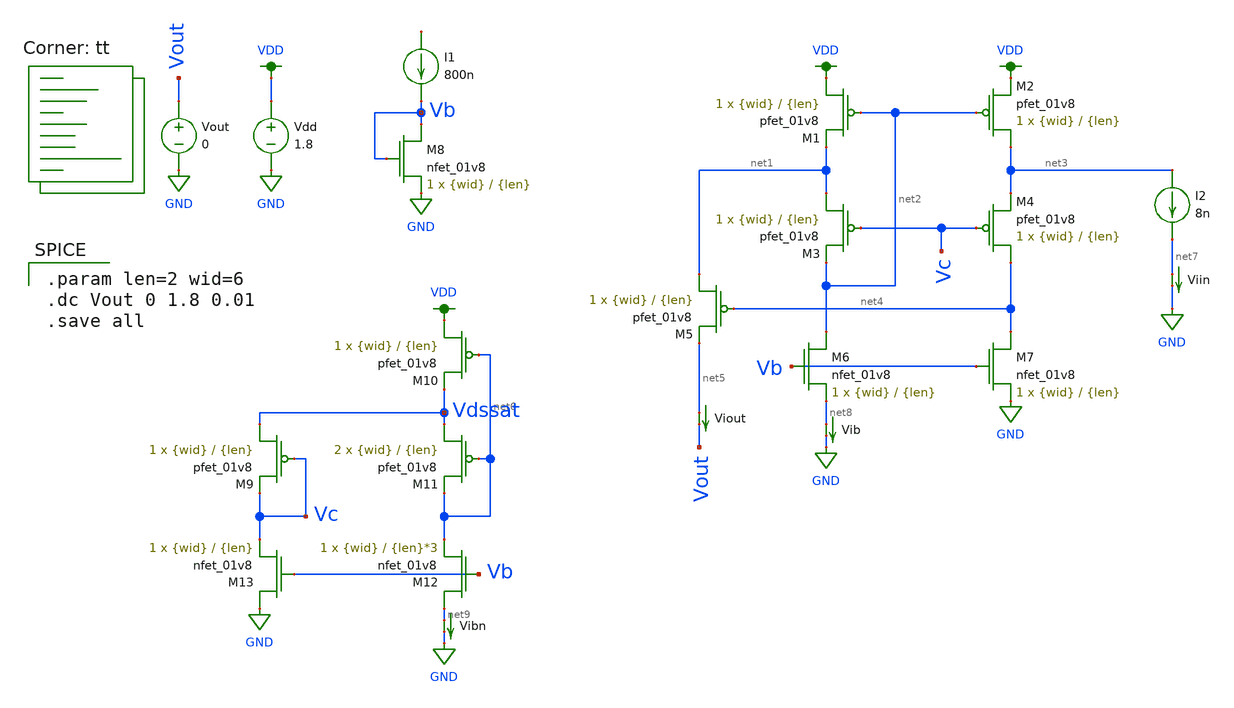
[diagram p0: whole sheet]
** sch_path: mp3/mirror_tb.sch
**.subckt mirror_tb
XM1 VDD net2 net1 VDD sky130_fd_pr__pfet_01v8 L={len} W={wid} nf=1 ad='int((nf+1)/2) * W/nf * 0.29' as='int((nf+2)/2) * W/nf * 0.29'
+ pd='2*int((nf+1)/2) * (W/nf + 0.29)' ps='2*int((nf+2)/2) * (W/nf + 0.29)' nrd='0.29 / W' nrs='0.29 / W'
+ sa=0 sb=0 sd=0 mult=1 m=1
XM2 net3 net2 VDD VDD sky130_fd_pr__pfet_01v8 L={len} W={wid} nf=1 ad='int((nf+1)/2) * W/nf * 0.29' as='int((nf+2)/2) * W/nf * 0.29'
+ pd='2*int((nf+1)/2) * (W/nf + 0.29)' ps='2*int((nf+2)/2) * (W/nf + 0.29)' nrd='0.29 / W' nrs='0.29 / W'
+ sa=0 sb=0 sd=0 mult=1 m=1
XM3 net1 Vc net2 VDD sky130_fd_pr__pfet_01v8 L={len} W={wid} nf=1 ad='int((nf+1)/2) * W/nf * 0.29' as='int((nf+2)/2) * W/nf * 0.29'
+ pd='2*int((nf+1)/2) * (W/nf + 0.29)' ps='2*int((nf+2)/2) * (W/nf + 0.29)' nrd='0.29 / W' nrs='0.29 / W'
+ sa=0 sb=0 sd=0 mult=1 m=1
XM4 net4 Vc net3 VDD sky130_fd_pr__pfet_01v8 L={len} W={wid} nf=1 ad='int((nf+1)/2) * W/nf * 0.29' as='int((nf+2)/2) * W/nf * 0.29'
+ pd='2*int((nf+1)/2) * (W/nf + 0.29)' ps='2*int((nf+2)/2) * (W/nf + 0.29)' nrd='0.29 / W' nrs='0.29 / W'
+ sa=0 sb=0 sd=0 mult=1 m=1
XM5 net1 net4 net5 VDD sky130_fd_pr__pfet_01v8 L={len} W={wid} nf=1 ad='int((nf+1)/2) * W/nf * 0.29'
+ as='int((nf+2)/2) * W/nf * 0.29' pd='2*int((nf+1)/2) * (W/nf + 0.29)' ps='2*int((nf+2)/2) * (W/nf + 0.29)'
+ nrd='0.29 / W' nrs='0.29 / W' sa=0 sb=0 sd=0 mult=1 m=1
XM6 net2 Vb net8 GND sky130_fd_pr__nfet_01v8 L={len} W={wid} nf=1 ad='int((nf+1)/2) * W/nf * 0.29' as='int((nf+2)/2) * W/nf * 0.29'
+ pd='2*int((nf+1)/2) * (W/nf + 0.29)' ps='2*int((nf+2)/2) * (W/nf + 0.29)' nrd='0.29 / W' nrs='0.29 / W'
+ sa=0 sb=0 sd=0 mult=1 m=1
XM7 net4 Vb GND GND sky130_fd_pr__nfet_01v8 L={len} W={wid} nf=1 ad='int((nf+1)/2) * W/nf * 0.29' as='int((nf+2)/2) * W/nf * 0.29'
+ pd='2*int((nf+1)/2) * (W/nf + 0.29)' ps='2*int((nf+2)/2) * (W/nf + 0.29)' nrd='0.29 / W' nrs='0.29 / W'
+ sa=0 sb=0 sd=0 mult=1 m=1
XM8 Vb Vb GND GND sky130_fd_pr__nfet_01v8 L={len} W={wid} nf=1 ad='int((nf+1)/2) * W/nf * 0.29' as='int((nf+2)/2) * W/nf * 0.29'
+ pd='2*int((nf+1)/2) * (W/nf + 0.29)' ps='2*int((nf+2)/2) * (W/nf + 0.29)' nrd='0.29 / W' nrs='0.29 / W'
+ sa=0 sb=0 sd=0 mult=1 m=1
I1 net10 Vb 800n
I2 net3 net7 8n
Viout net5 Vout 0
.save i(viout)
XM9 Vdssat Vc Vc VDD sky130_fd_pr__pfet_01v8 L={len} W={wid} nf=1 ad='int((nf+1)/2) * W/nf * 0.29' as='int((nf+2)/2) * W/nf * 0.29'
+ pd='2*int((nf+1)/2) * (W/nf + 0.29)' ps='2*int((nf+2)/2) * (W/nf + 0.29)' nrd='0.29 / W' nrs='0.29 / W'
+ sa=0 sb=0 sd=0 mult=1 m=1
XM10 VDD net6 Vdssat VDD sky130_fd_pr__pfet_01v8 L={len} W={wid} nf=1 ad='int((nf+1)/2) * W/nf * 0.29'
+ as='int((nf+2)/2) * W/nf * 0.29' pd='2*int((nf+1)/2) * (W/nf + 0.29)' ps='2*int((nf+2)/2) * (W/nf + 0.29)'
+ nrd='0.29 / W' nrs='0.29 / W' sa=0 sb=0 sd=0 mult=1 m=1
XM11 Vdssat net6 net6 VDD sky130_fd_pr__pfet_01v8 L={len} W={wid} nf=1 ad='int((nf+1)/2) * W/nf * 0.29'
+ as='int((nf+2)/2) * W/nf * 0.29' pd='2*int((nf+1)/2) * (W/nf + 0.29)' ps='2*int((nf+2)/2) * (W/nf + 0.29)'
+ nrd='0.29 / W' nrs='0.29 / W' sa=0 sb=0 sd=0 mult=2 m=2
XM12 net9 Vb net6 GND sky130_fd_pr__nfet_01v8 L={len}*3 W={wid} nf=1 ad='int((nf+1)/2) * W/nf * 0.29'
+ as='int((nf+2)/2) * W/nf * 0.29' pd='2*int((nf+1)/2) * (W/nf + 0.29)' ps='2*int((nf+2)/2) * (W/nf + 0.29)'
+ nrd='0.29 / W' nrs='0.29 / W' sa=0 sb=0 sd=0 mult=1 m=1
XM13 GND Vb Vc GND sky130_fd_pr__nfet_01v8 L={len} W={wid} nf=1 ad='int((nf+1)/2) * W/nf * 0.29' as='int((nf+2)/2) * W/nf * 0.29'
+ pd='2*int((nf+1)/2) * (W/nf + 0.29)' ps='2*int((nf+2)/2) * (W/nf + 0.29)' nrd='0.29 / W' nrs='0.29 / W'
+ sa=0 sb=0 sd=0 mult=1 m=1
Vdd VDD GND 1.8
Viin net7 GND 0
.save i(viin)
Vib net8 GND 0
.save i(vib)
Vibn net9 GND 0
.save i(vibn)
Vout Vout GND 0
**** begin user architecture code

.param len=2 wid=6
.dc Vout 0 1.8 0.01
.save all


.lib $::SKYWATER_MODELS/sky130.lib.spice tt
**** end user architecture code
**.ends
.GLOBAL GND
.GLOBAL VDD
.end
